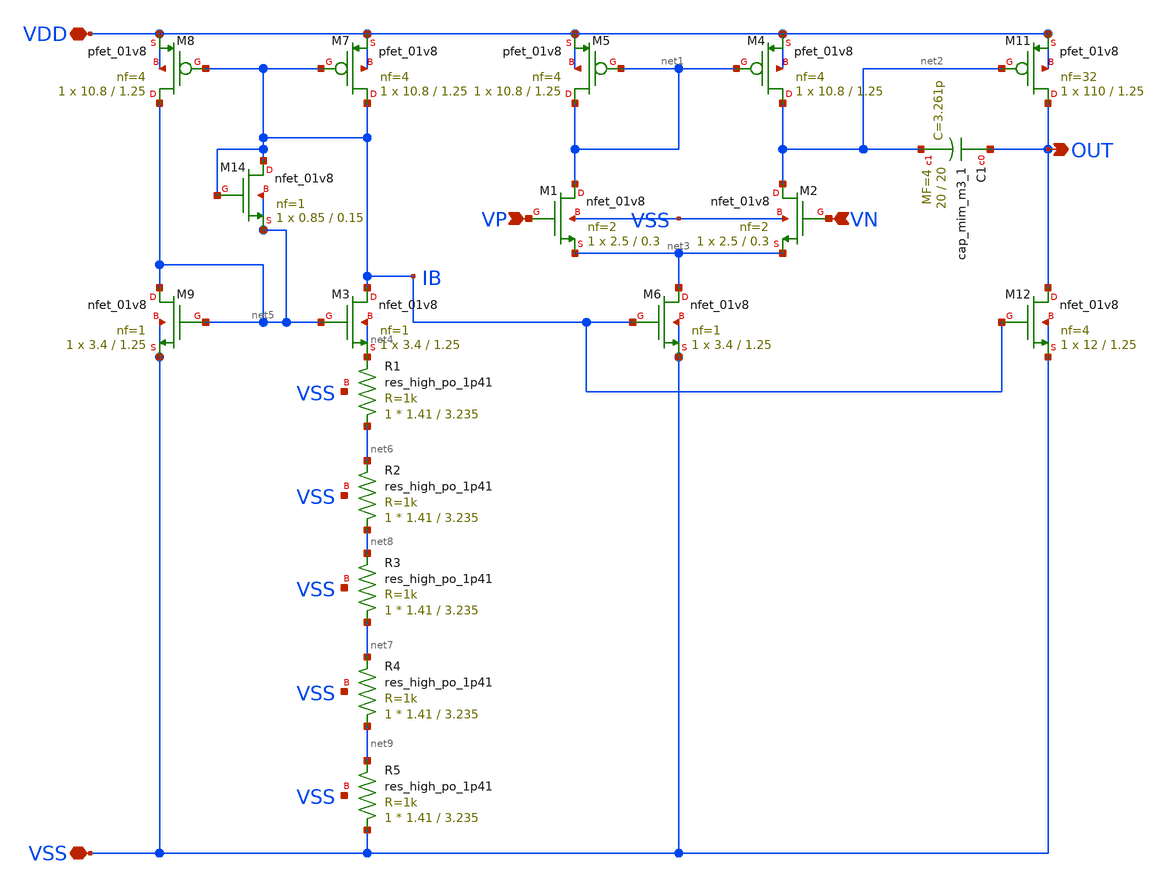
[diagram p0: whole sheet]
** sch_path: xschem/bandgap/bgr_ota/bgr-ota.sch
**.subckt bgr-ota VSS VDD VP VN OUT
*.iopin VSS
*.iopin VDD
*.ipin VP
*.ipin VN
*.opin OUT
XM1 net1 VP net3 VSS sky130_fd_pr__nfet_01v8 L=0.3 W=2.5 nf=2 ad='int((nf+1)/2) * W/nf * 0.29' as='int((nf+2)/2) * W/nf * 0.29'
+ pd='2*int((nf+1)/2) * (W/nf + 0.29)' ps='2*int((nf+2)/2) * (W/nf + 0.29)' nrd='0.29 / W' nrs='0.29 / W'
+ sa=0 sb=0 sd=0 mult=1 m=1
XM2 net2 VN net3 VSS sky130_fd_pr__nfet_01v8 L=0.3 W=2.5 nf=2 ad='int((nf+1)/2) * W/nf * 0.29' as='int((nf+2)/2) * W/nf * 0.29'
+ pd='2*int((nf+1)/2) * (W/nf + 0.29)' ps='2*int((nf+2)/2) * (W/nf + 0.29)' nrd='0.29 / W' nrs='0.29 / W'
+ sa=0 sb=0 sd=0 mult=1 m=1
XM4 net2 net1 VDD VDD sky130_fd_pr__pfet_01v8 L=1.25 W=10.8 nf=4 ad='int((nf+1)/2) * W/nf * 0.29' as='int((nf+2)/2) * W/nf * 0.29'
+ pd='2*int((nf+1)/2) * (W/nf + 0.29)' ps='2*int((nf+2)/2) * (W/nf + 0.29)' nrd='0.29 / W' nrs='0.29 / W'
+ sa=0 sb=0 sd=0 mult=1 m=1
XM5 net1 net1 VDD VDD sky130_fd_pr__pfet_01v8 L=1.25 W=10.8 nf=4 ad='int((nf+1)/2) * W/nf * 0.29' as='int((nf+2)/2) * W/nf * 0.29'
+ pd='2*int((nf+1)/2) * (W/nf + 0.29)' ps='2*int((nf+2)/2) * (W/nf + 0.29)' nrd='0.29 / W' nrs='0.29 / W'
+ sa=0 sb=0 sd=0 mult=1 m=1
XM6 net3 IB VSS VSS sky130_fd_pr__nfet_01v8 L=1.25 W=3.4 nf=1 ad='int((nf+1)/2) * W/nf * 0.29' as='int((nf+2)/2) * W/nf * 0.29'
+ pd='2*int((nf+1)/2) * (W/nf + 0.29)' ps='2*int((nf+2)/2) * (W/nf + 0.29)' nrd='0.29 / W' nrs='0.29 / W'
+ sa=0 sb=0 sd=0 mult=1 m=1
XM3 IB net5 net4 net4 sky130_fd_pr__nfet_01v8 L=1.25 W=3.4 nf=1 ad='int((nf+1)/2) * W/nf * 0.29' as='int((nf+2)/2) * W/nf * 0.29'
+ pd='2*int((nf+1)/2) * (W/nf + 0.29)' ps='2*int((nf+2)/2) * (W/nf + 0.29)' nrd='0.29 / W' nrs='0.29 / W'
+ sa=0 sb=0 sd=0 mult=1 m=1
XM7 IB IB VDD VDD sky130_fd_pr__pfet_01v8 L=1.25 W=10.8 nf=4 ad='int((nf+1)/2) * W/nf * 0.29' as='int((nf+2)/2) * W/nf * 0.29'
+ pd='2*int((nf+1)/2) * (W/nf + 0.29)' ps='2*int((nf+2)/2) * (W/nf + 0.29)' nrd='0.29 / W' nrs='0.29 / W'
+ sa=0 sb=0 sd=0 mult=1 m=1
XM8 net5 IB VDD VDD sky130_fd_pr__pfet_01v8 L=1.25 W=10.8 nf=4 ad='int((nf+1)/2) * W/nf * 0.29' as='int((nf+2)/2) * W/nf * 0.29'
+ pd='2*int((nf+1)/2) * (W/nf + 0.29)' ps='2*int((nf+2)/2) * (W/nf + 0.29)' nrd='0.29 / W' nrs='0.29 / W'
+ sa=0 sb=0 sd=0 mult=1 m=1
XM9 net5 net5 VSS VSS sky130_fd_pr__nfet_01v8 L=1.25 W=3.4 nf=1 ad='int((nf+1)/2) * W/nf * 0.29' as='int((nf+2)/2) * W/nf * 0.29'
+ pd='2*int((nf+1)/2) * (W/nf + 0.29)' ps='2*int((nf+2)/2) * (W/nf + 0.29)' nrd='0.29 / W' nrs='0.29 / W'
+ sa=0 sb=0 sd=0 mult=1 m=1
XM11 OUT net2 VDD VDD sky130_fd_pr__pfet_01v8 L=1.25 W=110 nf=32 ad='int((nf+1)/2) * W/nf * 0.29' as='int((nf+2)/2) * W/nf * 0.29'
+ pd='2*int((nf+1)/2) * (W/nf + 0.29)' ps='2*int((nf+2)/2) * (W/nf + 0.29)' nrd='0.29 / W' nrs='0.29 / W'
+ sa=0 sb=0 sd=0 mult=1 m=1
XM12 OUT IB VSS VSS sky130_fd_pr__nfet_01v8 L=1.25 W=12 nf=4 ad='int((nf+1)/2) * W/nf * 0.29' as='int((nf+2)/2) * W/nf * 0.29'
+ pd='2*int((nf+1)/2) * (W/nf + 0.29)' ps='2*int((nf+2)/2) * (W/nf + 0.29)' nrd='0.29 / W' nrs='0.29 / W'
+ sa=0 sb=0 sd=0 mult=1 m=1
XC1 OUT net2 sky130_fd_pr__cap_mim_m3_1 W=20 L=20 MF=4 m=4
XM14 IB IB net5 net5 sky130_fd_pr__nfet_01v8 L=0.15 W=0.85 nf=1 ad='int((nf+1)/2) * W/nf * 0.29' as='int((nf+2)/2) * W/nf * 0.29'
+ pd='2*int((nf+1)/2) * (W/nf + 0.29)' ps='2*int((nf+2)/2) * (W/nf + 0.29)' nrd='0.29 / W' nrs='0.29 / W'
+ sa=0 sb=0 sd=0 mult=1 m=1
XR1 net6 net4 VSS sky130_fd_pr__res_high_po_1p41 L=3.235 mult=1 m=1
XR2 net8 net6 VSS sky130_fd_pr__res_high_po_1p41 L=3.235 mult=1 m=1
XR3 net7 net8 VSS sky130_fd_pr__res_high_po_1p41 L=3.235 mult=1 m=1
XR4 net9 net7 VSS sky130_fd_pr__res_high_po_1p41 L=3.235 mult=1 m=1
XR5 VSS net9 VSS sky130_fd_pr__res_high_po_1p41 L=3.235 mult=1 m=1
**.ends
.end
